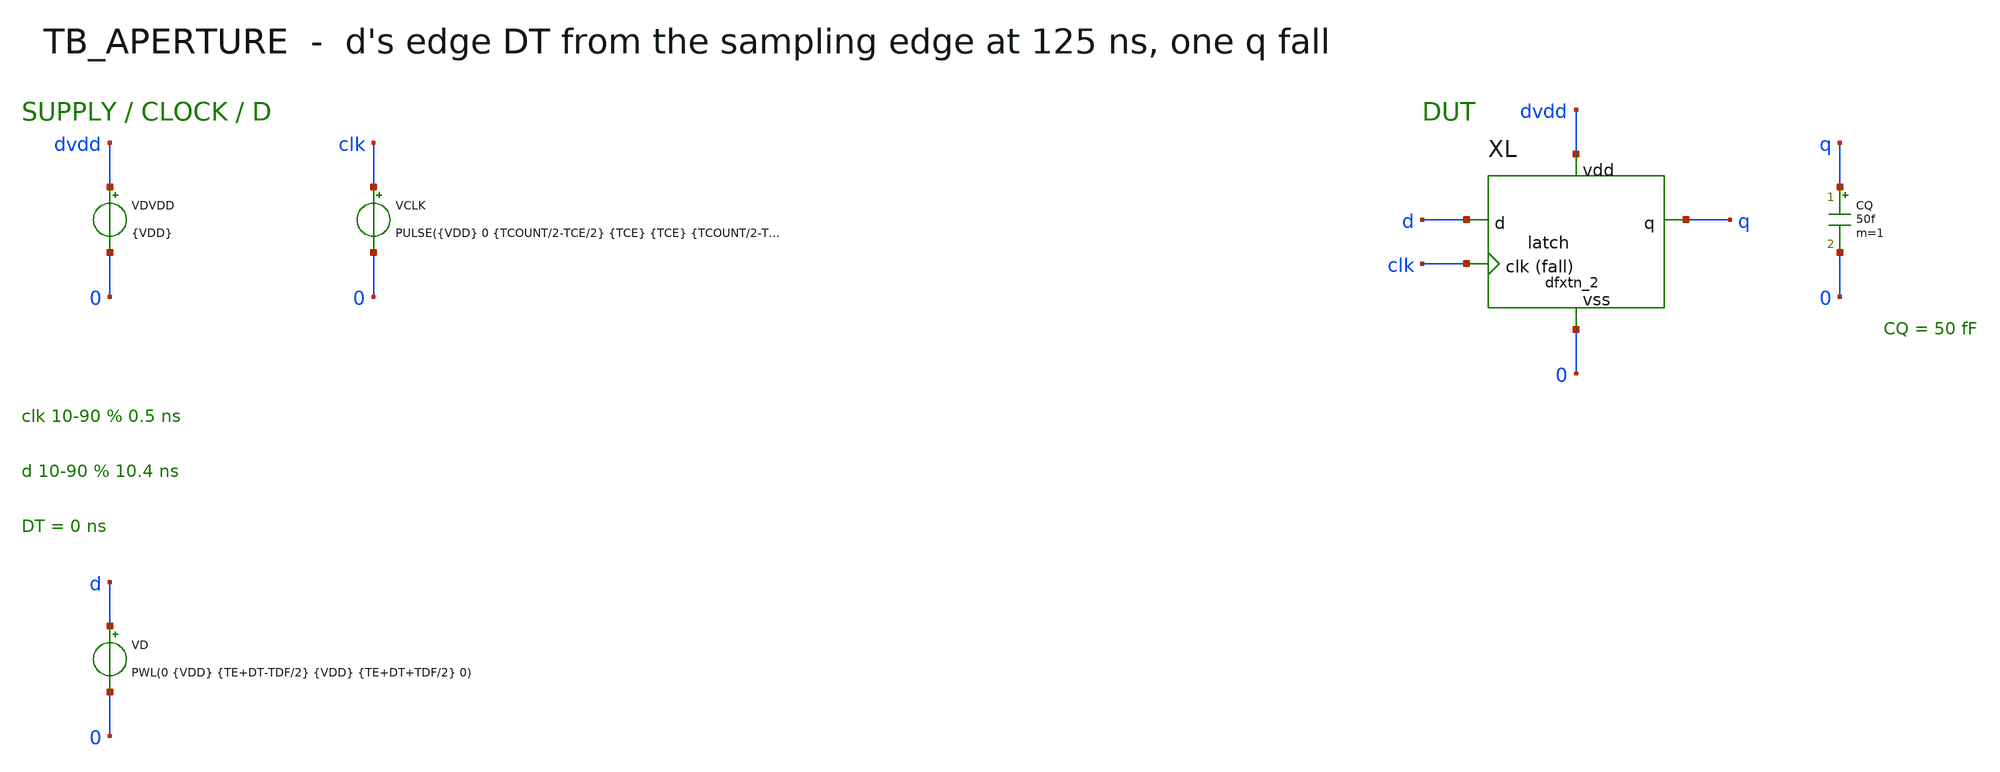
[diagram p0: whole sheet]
** sch_path: mixed_signal/latch/tb_aperture.sch
**.subckt tb_aperture
VDVDD dvdd 0 {VDD}
VCLK clk 0 PULSE({VDD} 0 {TCOUNT/2-TCE/2} {TCE} {TCE} {TCOUNT/2-TCE} {TCOUNT})
VD d 0 PWL(0 {VDD} {TE+DT-TDF/2} {VDD} {TE+DT+TDF/2} 0)
XL d clk q dvdd 0 latch
CQ q 0 50f m=1
**** begin user architecture code

.include /foss/pdks/gf180mcuD/libs.tech/ngspice/design.ngspice
.lib /foss/pdks/gf180mcuD/libs.tech/ngspice/sm141064.ngspice typical
.include /foss/pdk_libs/gf180mcuD/libs.ref/gf180mcu_as_sc_mcu7t3v3/spice/gf180mcu_as_sc_mcu7t3v3.spice
.param VDD=3.3
.param TCOUNT=50n
.param TCE=6.250000e-10
.param TDF=1.300000e-08
.param TE=125n
.param DT=0.000000000000000e+00
.param TSTOP=240n
.temp 27
.csparam cs_vdd={VDD}
.csparam cs_te={TE}
.csparam cs_tcount={TCOUNT}
.options reltol=1e-5 abstol=1e-13 vntol=1e-7
.tran 1p {TSTOP} 0 5p
.control
run
let half = $&cs_vdd / 2
let hi90 = 0.9 * $&cs_vdd
let lo10 = 0.1 * $&cs_vdd
meas tran t_q when v(q)=$&half fall=1 td=100e-9
meas tran t_q2 when v(q)=$&half fall=2 td=100e-9
meas tran t_qr when v(q)=$&half rise=1 td=100e-9
meas tran t_q90 when v(q)=$&hi90 fall=1 td=100e-9
meas tran t_q10 when v(q)=$&lo10 fall=1 td=100e-9
let t_edge = $&cs_te + floor((t_q - $&cs_te) / $&cs_tcount) * $&cs_tcount
let edge_k = (t_edge - $&cs_te) / $&cs_tcount
let tcq = t_q - t_edge
let q_fall = t_q10 - t_q90
set numdgt=10
echo RESULT_BEGIN
print tcq q_fall edge_k t_q
echo RESULT_END
quit
.endc

**** end user architecture code
**.ends

* expanding   symbol:  latch.sym # of pins=5
** sym_path: mixed_signal/latch/latch.sym
** sch_path: mixed_signal/latch/latch.sch
.subckt latch d clk q vdd vss
*.iopin vdd
*.iopin vss
*.ipin d
*.ipin clk
*.opin q
XFF vdd vdd vss vss clk d q gf180mcu_as_sc_mcu7t3v3__dfxtn_2
.ends

.end
